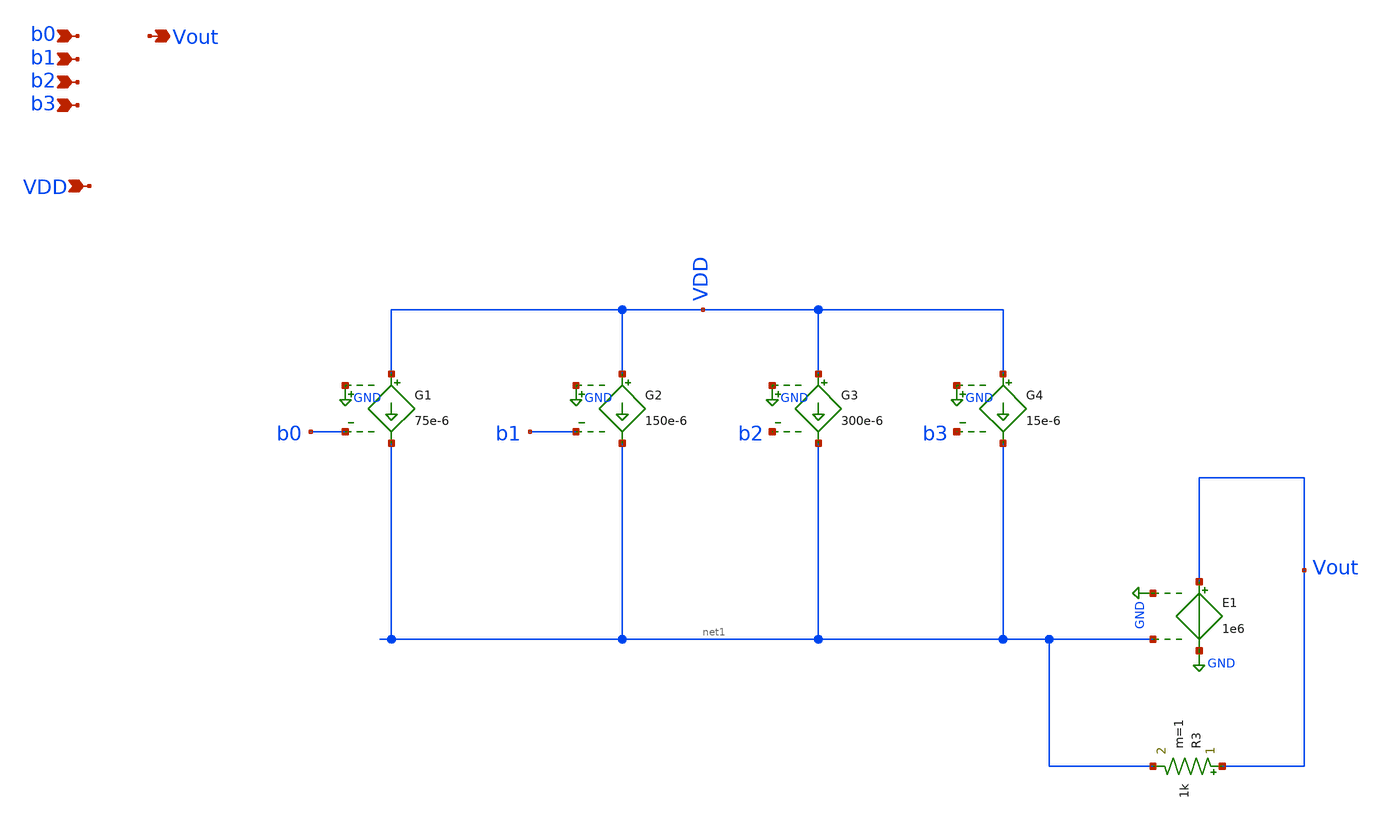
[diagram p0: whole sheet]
** sch_path: Ideal/IdealDAC.sch
**.subckt IdealDAC VDD b3 b2 b1 b0 Vout
*.ipin VDD
*.ipin b3
*.ipin b2
*.ipin b1
*.ipin b0
*.opin Vout
G1 VDD net1 GND b0 75e-6
G2 VDD net1 GND b1 150e-6
G3 VDD net1 GND b2 300e-6
G4 VDD net1 GND b3 15e-6
E1 Vout GND GND net1 1e6
R3 Vout net1 1k m=1
**.ends
.GLOBAL GND
.end
